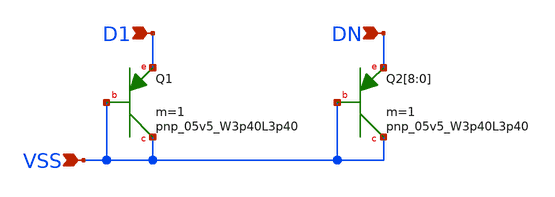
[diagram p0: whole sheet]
** sch_path: design/LELO_GR02_SKY130A/BANDGAP_DIODE.sch
**.subckt BANDGAP_DIODE VSS D1 DN
*.ipin VSS
*.ipin D1
*.ipin DN
XQ1 VSS VSS D1 sky130_fd_pr__pnp_05v5_W3p40L3p40 m=1
XQ2[8] VSS VSS DN sky130_fd_pr__pnp_05v5_W3p40L3p40 m=1
XQ2[7] VSS VSS DN sky130_fd_pr__pnp_05v5_W3p40L3p40 m=1
XQ2[6] VSS VSS DN sky130_fd_pr__pnp_05v5_W3p40L3p40 m=1
XQ2[5] VSS VSS DN sky130_fd_pr__pnp_05v5_W3p40L3p40 m=1
XQ2[4] VSS VSS DN sky130_fd_pr__pnp_05v5_W3p40L3p40 m=1
XQ2[3] VSS VSS DN sky130_fd_pr__pnp_05v5_W3p40L3p40 m=1
XQ2[2] VSS VSS DN sky130_fd_pr__pnp_05v5_W3p40L3p40 m=1
XQ2[1] VSS VSS DN sky130_fd_pr__pnp_05v5_W3p40L3p40 m=1
XQ2[0] VSS VSS DN sky130_fd_pr__pnp_05v5_W3p40L3p40 m=1
**.ends
.end
